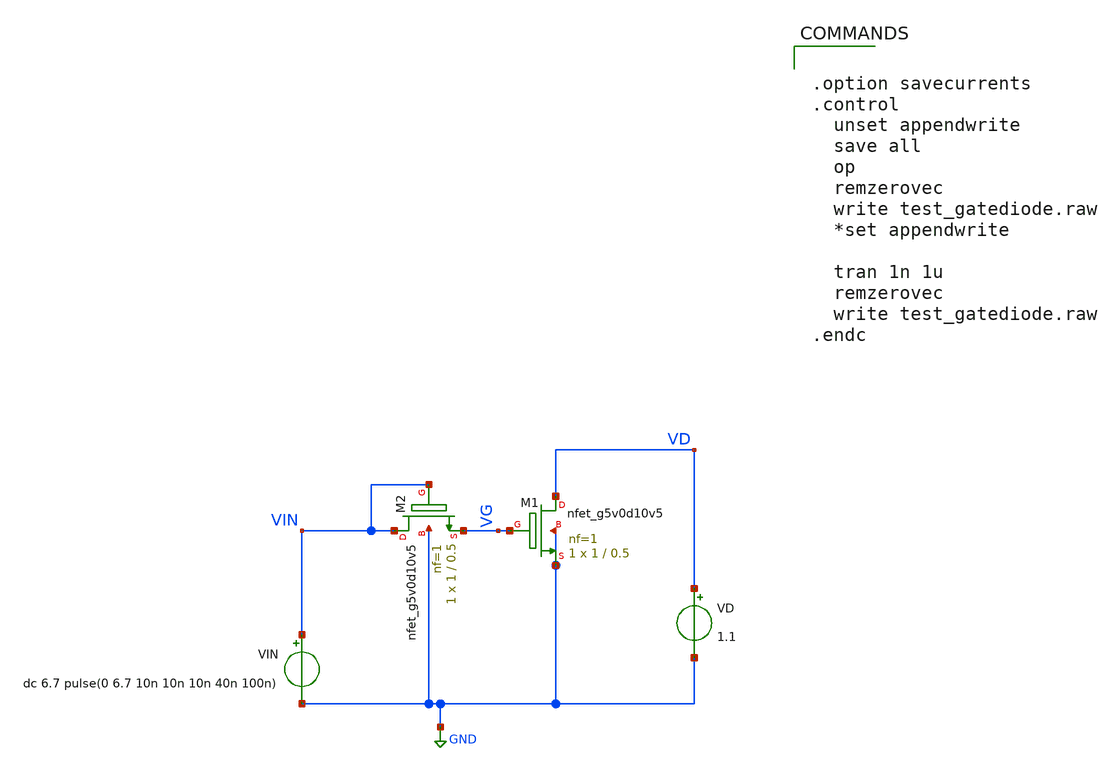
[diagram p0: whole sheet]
** sch_path: row_drivers/test_gatediode.sch
**.subckt test_gatediode
XM1 VD VG GND GND sky130_fd_pr__nfet_g5v0d10v5 L=0.5 W=1 nf=1 ad='int((nf+1)/2) * W/nf * 0.29' as='int((nf+2)/2) * W/nf * 0.29'
+ pd='2*int((nf+1)/2) * (W/nf + 0.29)' ps='2*int((nf+2)/2) * (W/nf + 0.29)' nrd='0.29 / W' nrs='0.29 / W'
+ sa=0 sb=0 sd=0 mult=1 m=1
XM2 VIN VIN VG GND sky130_fd_pr__nfet_g5v0d10v5 L=0.5 W=1 nf=1 ad='int((nf+1)/2) * W/nf * 0.29' as='int((nf+2)/2) * W/nf * 0.29'
+ pd='2*int((nf+1)/2) * (W/nf + 0.29)' ps='2*int((nf+2)/2) * (W/nf + 0.29)' nrd='0.29 / W' nrs='0.29 / W'
+ sa=0 sb=0 sd=0 mult=1 m=1
VIN VIN GND dc 6.7 pulse(0 6.7 10n 10n 10n 40n 100n)
VD VD GND 1.1
**** begin user architecture code

** opencircuitdesign pdks install
.lib $::SKYWATER_MODELS/sky130.lib.spice tt




.option savecurrents
.control
  unset appendwrite
  save all
  op
  remzerovec
  write test_gatediode.raw
  *set appendwrite

  tran 1n 1u
  remzerovec
  write test_gatediode.raw
.endc


**** end user architecture code
**.ends
.GLOBAL GND
.end
